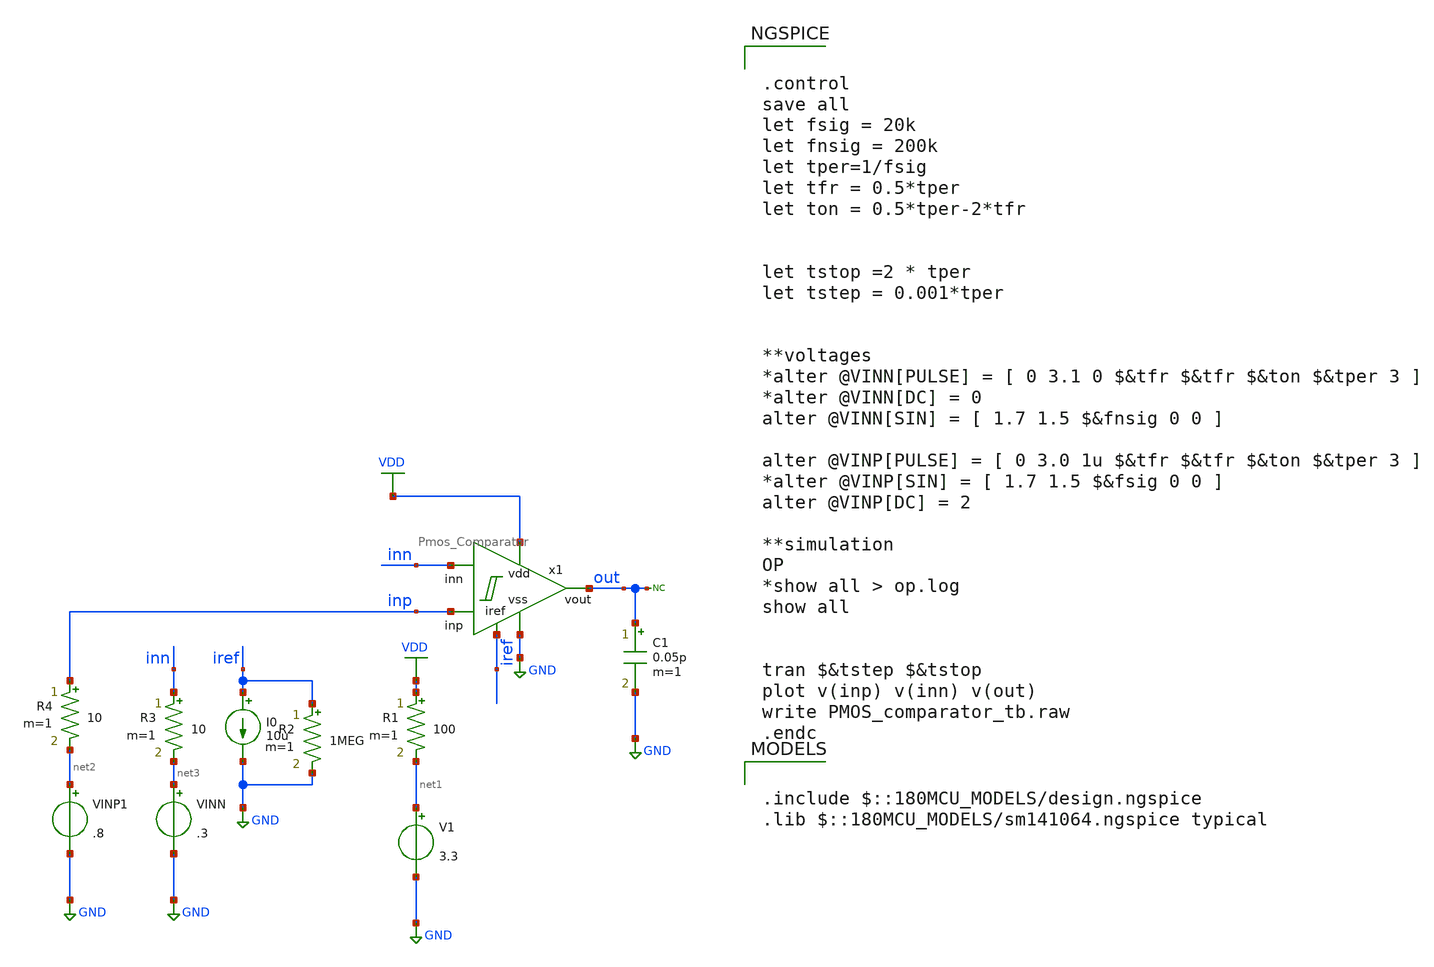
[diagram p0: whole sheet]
** sch_path: designs/libs/tb_analog_pads_pex/tb_Comparator/PMOS_comparator_tb.sch
**.subckt PMOS_comparator_tb
I0 iref GND 10u
V1 net1 GND 3.3
VINN net3 GND .3
* noconn out
VINP1 net2 GND .8
x1 VDD out inp GND inn iref Pmos_Comparator
R1 VDD net1 100 m=1
R2 iref GND 1MEG m=1
R3 inn net3 10 m=1
R4 inp net2 10 m=1
C1 out GND 0.05p m=1
**** begin user architecture code


.control
save all
let fsig = 20k
let fnsig = 200k
let tper=1/fsig
let tfr = 0.5*tper
let ton = 0.5*tper-2*tfr


let tstop =2 * tper
let tstep = 0.001*tper


**voltages
*alter @VINN[PULSE] = [ 0 3.1 0 $&tfr $&tfr $&ton $&tper 3 ]
*alter @VINN[DC] = 0
alter @VINN[SIN] = [ 1.7 1.5 $&fnsig 0 0 ]

alter @VINP[PULSE] = [ 0 3.0 1u $&tfr $&tfr $&ton $&tper 3 ]
*alter @VINP[SIN] = [ 1.7 1.5 $&fsig 0 0 ]
alter @VINP[DC] = 2

**simulation
OP
*show all > op.log
show all


tran $&tstep $&tstop
plot v(inp) v(inn) v(out)
write PMOS_comparator_tb.raw
.endc



.include $::180MCU_MODELS/design.ngspice
.lib $::180MCU_MODELS/sm141064.ngspice typical

**** end user architecture code
**.ends
.GLOBAL GND
.GLOBAL VDD
.end
